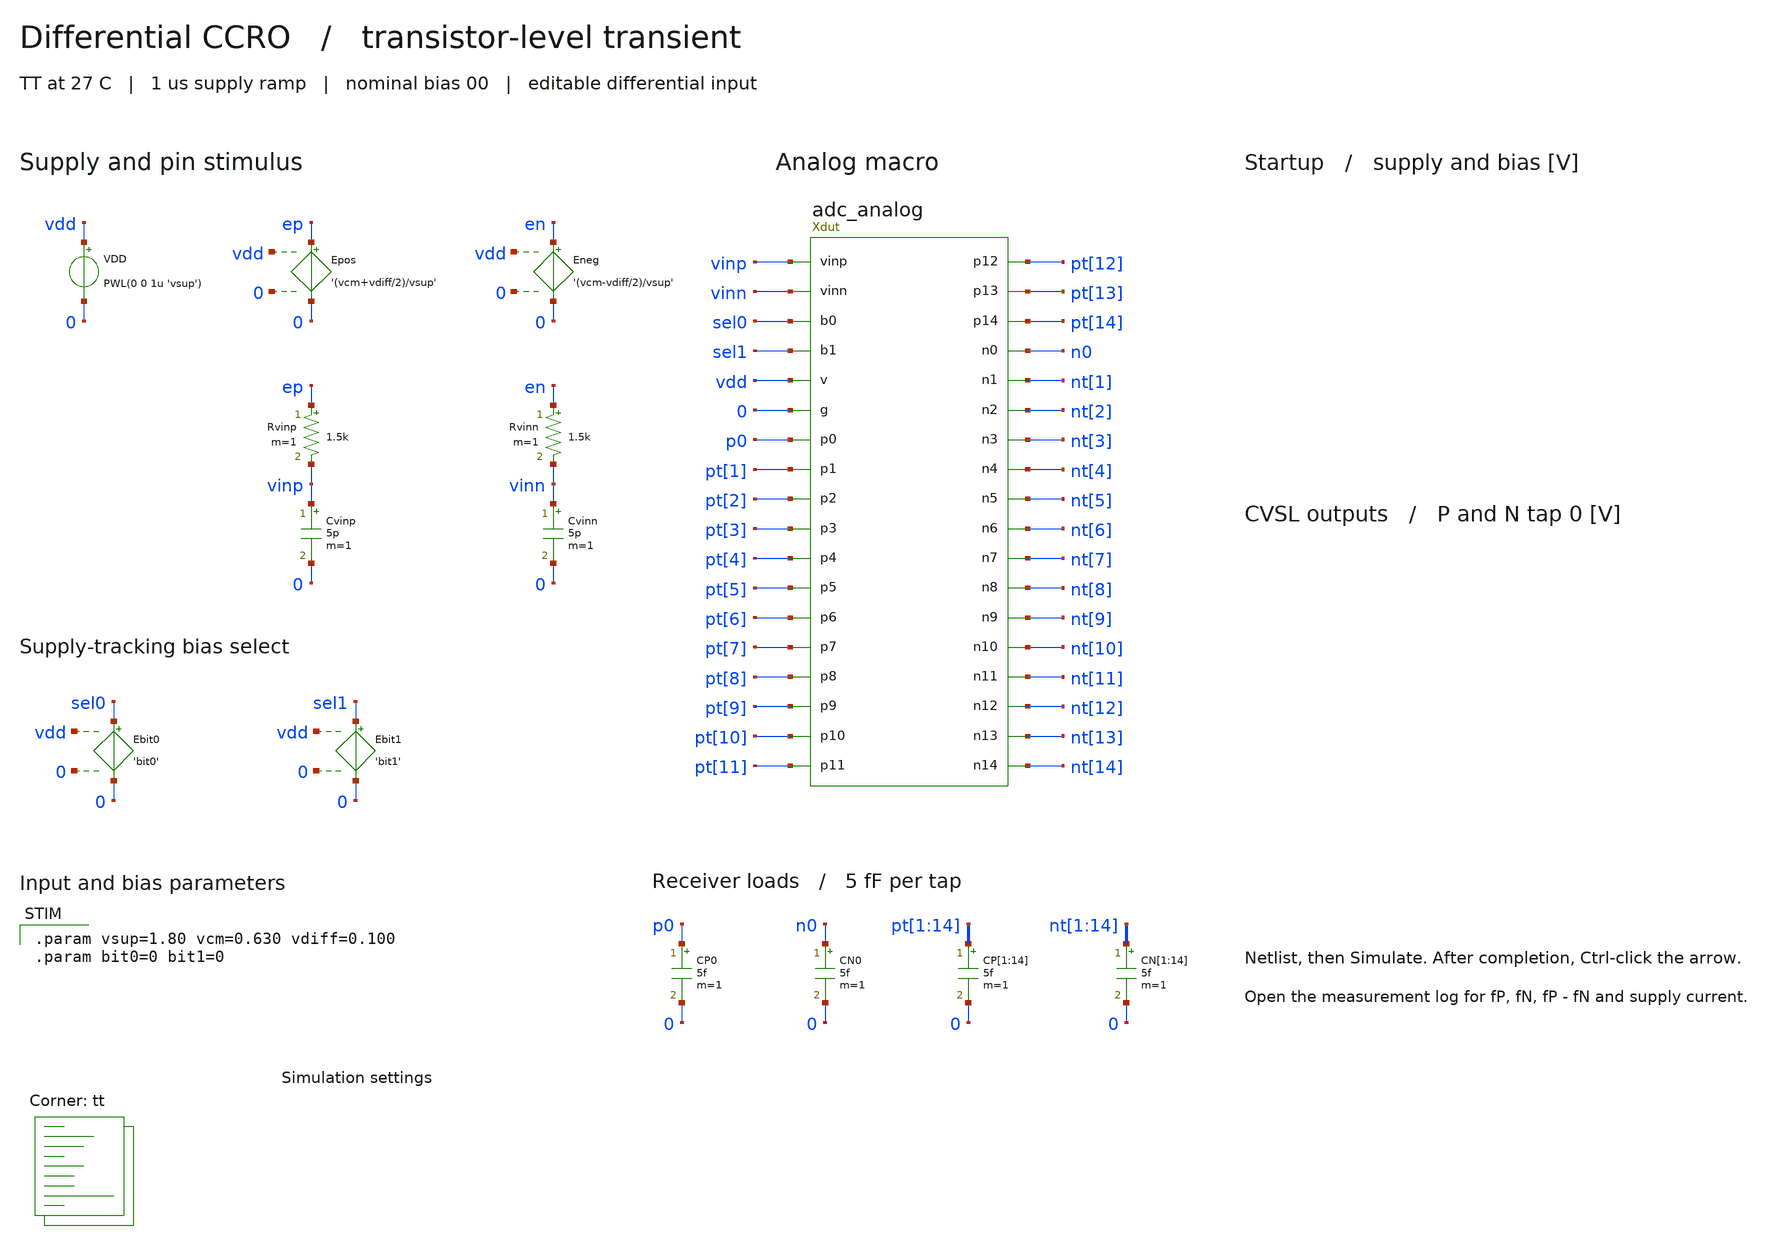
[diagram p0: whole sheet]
** sch_path: review/bench/tb_ccro.sch
**.subckt tb_ccro
VDD vdd 0 PWL(0 0 1u 'vsup')
Epos ep 0 vdd 0 '(vcm+vdiff/2)/vsup'
Eneg en 0 vdd 0 '(vcm-vdiff/2)/vsup'
Rvinp ep vinp 1.5k m=1
Cvinp vinp 0 5p m=1
Rvinn en vinn 1.5k m=1
Cvinn vinn 0 5p m=1
Ebit0 sel0 0 vdd 0 'bit0'
Ebit1 sel1 0 vdd 0 'bit1'
Xdut vinp vinn sel0 sel1 vdd 0 p0 pt[1] pt[2] pt[3] pt[4] pt[5] pt[6] pt[7] pt[8] pt[9] pt[10]
+ pt[11] pt[12] pt[13] pt[14] n0 nt[1] nt[2] nt[3] nt[4] nt[5] nt[6] nt[7] nt[8] nt[9] nt[10] nt[11] nt[12]
+ nt[13] nt[14] adc_analog
CP0 p0 0 5f m=1
CN0 n0 0 5f m=1
CP[1] pt[1] 0 5f m=1
CP[2] pt[2] 0 5f m=1
CP[3] pt[3] 0 5f m=1
CP[4] pt[4] 0 5f m=1
CP[5] pt[5] 0 5f m=1
CP[6] pt[6] 0 5f m=1
CP[7] pt[7] 0 5f m=1
CP[8] pt[8] 0 5f m=1
CP[9] pt[9] 0 5f m=1
CP[10] pt[10] 0 5f m=1
CP[11] pt[11] 0 5f m=1
CP[12] pt[12] 0 5f m=1
CP[13] pt[13] 0 5f m=1
CP[14] pt[14] 0 5f m=1
CN[1] nt[1] 0 5f m=1
CN[2] nt[2] 0 5f m=1
CN[3] nt[3] 0 5f m=1
CN[4] nt[4] 0 5f m=1
CN[5] nt[5] 0 5f m=1
CN[6] nt[6] 0 5f m=1
CN[7] nt[7] 0 5f m=1
CN[8] nt[8] 0 5f m=1
CN[9] nt[9] 0 5f m=1
CN[10] nt[10] 0 5f m=1
CN[11] nt[11] 0 5f m=1
CN[12] nt[12] 0 5f m=1
CN[13] nt[13] 0 5f m=1
CN[14] nt[14] 0 5f m=1
**** begin user architecture code

.param vsup=1.80 vcm=0.630 vdiff=0.100
.param bit0=0 bit1=0

.lib $::SKYWATER_MODELS/sky130.lib.spice tt

.option scale=1u method=gear reltol=0.0005
.temp 27
.csparam stop_s='8u+22u*bit0*(1-bit1)'
.control
set num_threads=1
save v(vdd) v(vinp) v(vinn) v(xdut.xf.vb) v(xdut.rp) v(xdut.rn) v(p0) v(n0) i(vdd)
set tstop = $&stop_s
tran 2n $tstop 0 2n
if time[length(time)-1] < 0.999999*$tstop
  echo Incomplete transient
  quit 2
end
meas tran period2p TRIG v(p0) VAL=0.9 TD=5u RISE=1 TARG v(p0) VAL=0.9 TD=5u RISE=3
meas tran period2n TRIG v(n0) VAL=0.9 TD=5u RISE=1 TARG v(n0) VAL=0.9 TD=5u RISE=3
meas tran supply_a AVG i(vdd) FROM=5u TO=$tstop
let fp_mhz = 2e-6/period2p
let fn_mhz = 2e-6/period2n
let delta_mhz = fp_mhz-fn_mhz
let idd_ua = -1e6*supply_a
print fp_mhz fn_mhz delta_mhz idd_ua
write tb_ccro.raw time v(vdd) v(vinp) v(vinn) v(xdut.xf.vb) v(xdut.rp) v(xdut.rn) v(p0) v(n0) i(vdd)
quit
.endc

**** end user architecture code
**.ends
.end
